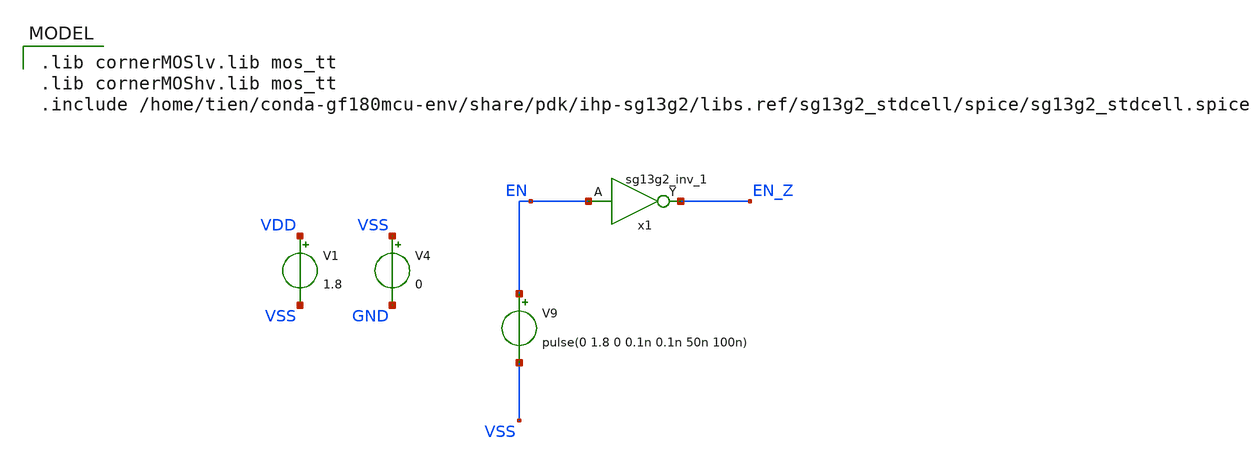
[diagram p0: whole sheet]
** sch_path: schematic/test-inv.sch
**.subckt test-inv
x1 EN_Z EN VDD VSS sg13g2_inv_1
V9 EN VSS pulse(0 1.8 0 0.1n 0.1n 50n 100n)
V1 VDD VSS 1.8
.save i(v1)
V4 VSS GND 0
**** begin user architecture code
 .lib cornerMOSlv.lib mos_tt
.lib cornerMOShv.lib mos_tt
.include /home/tien/conda-gf180mcu-env/share/pdk/ihp-sg13g2/libs.ref/sg13g2_stdcell/spice/sg13g2_stdcell.spice




.option temp = 27
.save all

.option GMIN=1e-12 reltol=1e-6

.tran 10n 100u


**** end user architecture code
**.ends

* expanding   symbol:  sg13g2_stdcells/sg13g2_inv_1.sym # of pins=2
** sym_path: sg13g2_stdcells/sg13g2_inv_1.sym
** sch_path: sg13g2_stdcells/sg13g2_inv_1.sch
.subckt sg13g2_inv_1 Y A VDD VSS
*.opin Y
*.ipin A
*.iopin VDD
*.iopin VSS
XM1 Y A VSS VSS sg13_lv_nmos w=740.00n l=130.00n ng=1 m=1 mm_ok=1
XM2 Y A VDD VDD sg13_lv_pmos w=1.12u l=130.00n ng=1 m=1 mm_ok=1
.ends

.end
